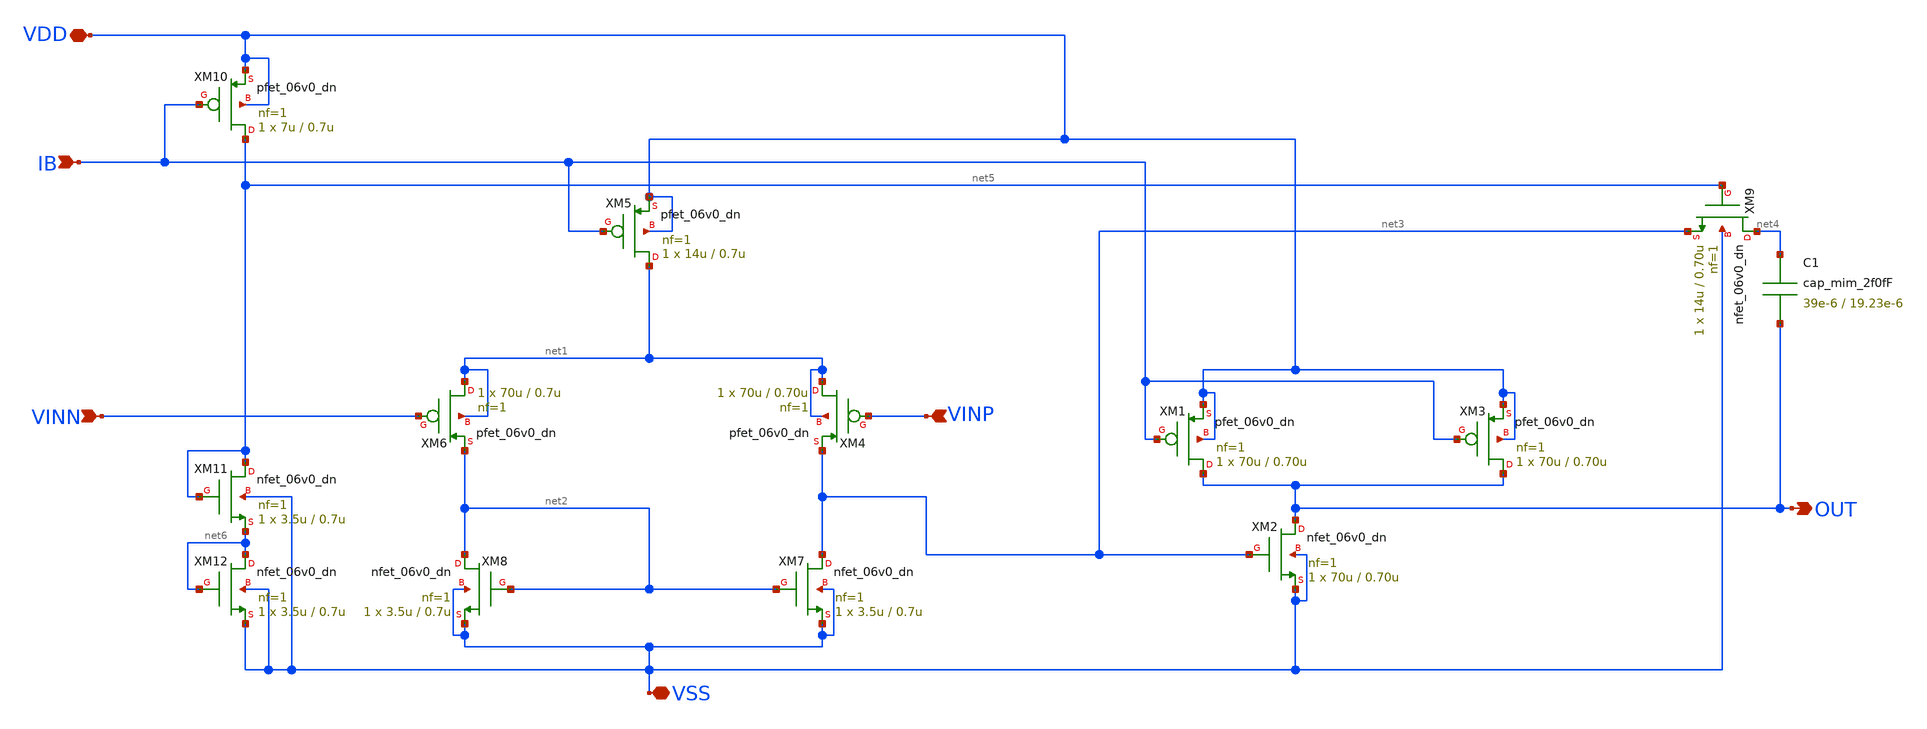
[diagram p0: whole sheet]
** sch_path: member_project/gitefu/op_20231204_flat.sch
**.subckt op_20231204_flat OUT VDD IB VINN VINP VSS
*.opin OUT
*.iopin VDD
*.ipin IB
*.ipin VINN
*.ipin VINP
*.iopin VSS
XM1 OUT IB VDD VDD pfet_06v0_dn L=0.70u W=70u nf=1 ad='int((nf+1)/2) * W/nf * 0.18u' as='int((nf+2)/2) * W/nf * 0.18u'
+ pd='2*int((nf+1)/2) * (W/nf + 0.18u)' ps='2*int((nf+2)/2) * (W/nf + 0.18u)' nrd='0.18u / W' nrs='0.18u / W'
+ sa=0 sb=0 sd=0 m=1
XM2 OUT net3 VSS VSS nfet_06v0_dn L=0.70u W=70u nf=1 ad='int((nf+1)/2) * W/nf * 0.18u' as='int((nf+2)/2) * W/nf * 0.18u'
+ pd='2*int((nf+1)/2) * (W/nf + 0.18u)' ps='2*int((nf+2)/2) * (W/nf + 0.18u)' nrd='0.18u / W' nrs='0.18u / W'
+ sa=0 sb=0 sd=0 m=1
XM3 OUT IB VDD VDD pfet_06v0_dn L=0.70u W=70u nf=1 ad='int((nf+1)/2) * W/nf * 0.18u' as='int((nf+2)/2) * W/nf * 0.18u'
+ pd='2*int((nf+1)/2) * (W/nf + 0.18u)' ps='2*int((nf+2)/2) * (W/nf + 0.18u)' nrd='0.18u / W' nrs='0.18u / W'
+ sa=0 sb=0 sd=0 m=1
XM6 net1 VINN net2 net1 pfet_06v0_dn L=0.7u W=70u nf=1 ad='int((nf+1)/2) * W/nf * 0.18u' as='int((nf+2)/2) * W/nf * 0.18u'
+ pd='2*int((nf+1)/2) * (W/nf + 0.18u)' ps='2*int((nf+2)/2) * (W/nf + 0.18u)' nrd='0.18u / W' nrs='0.18u / W'
+ sa=0 sb=0 sd=0 m=1
XM4 net1 VINP net3 net1 pfet_06v0_dn L=0.70u W=70u nf=1 ad='int((nf+1)/2) * W/nf * 0.18u' as='int((nf+2)/2) * W/nf * 0.18u'
+ pd='2*int((nf+1)/2) * (W/nf + 0.18u)' ps='2*int((nf+2)/2) * (W/nf + 0.18u)' nrd='0.18u / W' nrs='0.18u / W'
+ sa=0 sb=0 sd=0 m=1
XM5 net1 IB VDD VDD pfet_06v0_dn L=0.7u W=14u nf=1 ad='int((nf+1)/2) * W/nf * 0.18u' as='int((nf+2)/2) * W/nf * 0.18u'
+ pd='2*int((nf+1)/2) * (W/nf + 0.18u)' ps='2*int((nf+2)/2) * (W/nf + 0.18u)' nrd='0.18u / W' nrs='0.18u / W'
+ sa=0 sb=0 sd=0 m=1
XM7 net3 net2 VSS VSS nfet_06v0_dn L=0.7u W=3.5u nf=1 ad='int((nf+1)/2) * W/nf * 0.18u' as='int((nf+2)/2) * W/nf * 0.18u'
+ pd='2*int((nf+1)/2) * (W/nf + 0.18u)' ps='2*int((nf+2)/2) * (W/nf + 0.18u)' nrd='0.18u / W' nrs='0.18u / W'
+ sa=0 sb=0 sd=0 m=1
XM8 net2 net2 VSS VSS nfet_06v0_dn L=0.7u W=3.5u nf=1 ad='int((nf+1)/2) * W/nf * 0.18u' as='int((nf+2)/2) * W/nf * 0.18u'
+ pd='2*int((nf+1)/2) * (W/nf + 0.18u)' ps='2*int((nf+2)/2) * (W/nf + 0.18u)' nrd='0.18u / W' nrs='0.18u / W'
+ sa=0 sb=0 sd=0 m=1
XM9 net4 net5 net3 VSS nfet_06v0_dn L=0.70u W=14u nf=1 ad='int((nf+1)/2) * W/nf * 0.18u' as='int((nf+2)/2) * W/nf * 0.18u'
+ pd='2*int((nf+1)/2) * (W/nf + 0.18u)' ps='2*int((nf+2)/2) * (W/nf + 0.18u)' nrd='0.18u / W' nrs='0.18u / W'
+ sa=0 sb=0 sd=0 m=1
XM11 net5 net5 net6 VSS nfet_06v0_dn L=0.7u W=3.5u nf=1 ad='int((nf+1)/2) * W/nf * 0.18u' as='int((nf+2)/2) * W/nf * 0.18u'
+ pd='2*int((nf+1)/2) * (W/nf + 0.18u)' ps='2*int((nf+2)/2) * (W/nf + 0.18u)' nrd='0.18u / W' nrs='0.18u / W'
+ sa=0 sb=0 sd=0 m=1
XM12 net6 net6 VSS VSS nfet_06v0_dn L=0.7u W=3.5u nf=1 ad='int((nf+1)/2) * W/nf * 0.18u' as='int((nf+2)/2) * W/nf * 0.18u'
+ pd='2*int((nf+1)/2) * (W/nf + 0.18u)' ps='2*int((nf+2)/2) * (W/nf + 0.18u)' nrd='0.18u / W' nrs='0.18u / W'
+ sa=0 sb=0 sd=0 m=1
XM10 net5 IB VDD VDD pfet_06v0_dn L=0.7u W=7u nf=1 ad='int((nf+1)/2) * W/nf * 0.18u' as='int((nf+2)/2) * W/nf * 0.18u'
+ pd='2*int((nf+1)/2) * (W/nf + 0.18u)' ps='2*int((nf+2)/2) * (W/nf + 0.18u)' nrd='0.18u / W' nrs='0.18u / W'
+ sa=0 sb=0 sd=0 m=1
C1 net4 OUT cap_mim_2f0fF W=39e-6 L=19.23e-6
**.ends
.end
